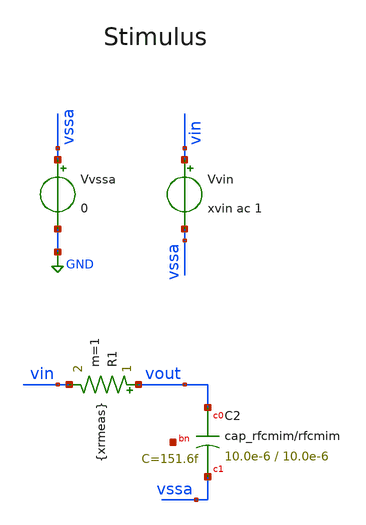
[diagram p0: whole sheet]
** sch_path: tb_cap_ihp/tb_cap_ihp.sch
**.subckt tb_cap_ihp
R1 vout vin {xrmeas} m=1
Vvssa vssa GND 0
Vvin vin vssa xvin ac 1
XC2 vout vssa net1 cap_rfcmim w=10.0e-6 l=10.0e-6 wfeed=5.0e-6 m=1 mm_ok=1
**** begin user architecture code

** opencircuitdesign pdks install
.lib /home/slice/pdk/iHP/IHP-Open-PDK/ihp-sg13g2/libs.tech/ngspice/models/cornerMOSlv.lib mos_tt
.lib /home/slice/pdk/iHP/IHP-Open-PDK/ihp-sg13g2/libs.tech/ngspice/models/cornerMOShv.lib mos_tt
.lib /home/slice/pdk/iHP/IHP-Open-PDK/ihp-sg13g2/libs.tech/ngspice/models/cornerCAP.lib cap_typ


* Parameters
.param xvin = -3.4
.param xrmeas = 1k
.param xCval = 1p
.csparam xvin_var = 'xvin'
.csparam xrmeas_var = 'xrmeas'
.temp 27


  ** must save the below for DCOP analysis to be back annotated onto the schematic
  .option savecurrents

  .include tb_cmeas_ihp.save

  *.save all
  .save v(vin) v(vout)
  .save @n.xm1.nsg13_lv_nmos[ids] @n.xm2.nsg13_hv_nmos[ids] @n.xm3.nsg13_lv_pmos[ids] @n.xm4.nsg13_hv_pmos[ids]

  .control

  *set xTj = ( -40 -30 -20 -10 0 10 20 30 40 50 60 70 80 90 100 110 120 130 )
  set xTj = ( 27 )
  foreach xTj_var $xTj

  let Tj_meas = $xTj_var

  echo temperature is "$&Tj_meas"

  set temp = $xTj_var


  ** 1. AC ANALYSIS **

  ac dec 10 1 1000G
  remzerovec
  write tb_cap_ihp.raw

  ** 2. MEASURES **

  let n45_rads = -45*(pi/180)
  echo "$&n45_rads"
  meas AC BW WHEN vp(vout)=n45_rads CROSS=1
  echo "$&BW"
  echo --
  let cmeas = 1/(2*pi*xrmeas_var*BW)
  echo "$&cmeas"
  echo "$&cmeas" >> cap_measures_typ.txt

  end

  setplot
*quit 0
.endc




**** end user architecture code
**.ends
.GLOBAL GND
.end
